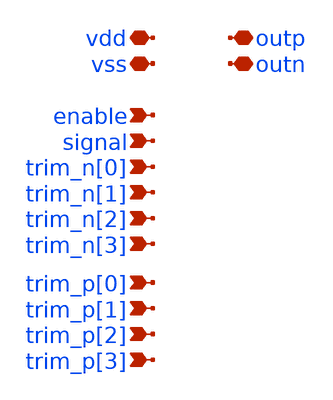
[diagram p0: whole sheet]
** sch_path: xschem/injector_pex_19_8.sch
**.subckt injector_pex_19_8 enable signal trim_n[0] trim_n[1] trim_n[2] trim_n[3] trim_p[0]
*+ trim_p[1] trim_p[2] trim_p[3] vss vdd outp outn
*.ipin enable
*.ipin signal
*.ipin trim_n[0]
*.ipin trim_n[1]
*.ipin trim_n[2]
*.ipin trim_n[3]
*.ipin trim_p[0]
*.ipin trim_p[1]
*.ipin trim_p[2]
*.ipin trim_p[3]
*.iopin vss
*.iopin vdd
*.iopin outp
*.iopin outn
**** begin user architecture code

* NGSPICE file created from injector_flat.ext - technology: gf180mcuC

.subckt injector_flat enable outn outp signal trim_n[0] trim_n[1] trim_n[2] trim_n[3]  trim_p[0]
+ trim_p[1] trim_p[2] trim_p[3] vss vdd
X0 vdd a_9644_7080# a_9556_7124# vdd pmos_6p0 w=1.22u l=1u
X1 outn _00_ vss vss nmos_6p0 w=0.82u l=0.6u
X2 vdd _21_ a_2500_4539# vdd pmos_6p0 w=0.62u l=0.5u
X3 outn _00_ vdd vdd pmos_6p0 w=1.22u l=0.5u
X4 a_2588_5512# a_2500_5556# vss vss nmos_6p0 w=0.82u l=1u
X5 _25_ a_6509_3160# vdd vdd pmos_6p0 w=1.22u l=0.5u
X6 vdd a_3036_5079# a_2948_5176# vdd pmos_6p0 w=1.22u l=1u
X7 a_3044_3229# a_2612_3229# vss vss nmos_6p0 w=0.36u l=0.6u
X8 outp _00_ vdd vdd pmos_6p0 w=1.22u l=0.5u
X9 outp _14_ vdd vdd pmos_6p0 w=1.22u l=0.5u
X10 outn _00_ vss vss nmos_6p0 w=0.82u l=0.6u
X11 vdd _00_ outn vdd pmos_6p0 w=1.22u l=0.5u
X12 vdd _24_ a_7092_3229# vdd pmos_6p0 w=0.62u l=0.5u
X13 vss trim_p[1] a_7204_7933# vss nmos_6p0 w=0.36u l=0.6u
X14 outp _00_ vdd vdd pmos_6p0 w=1.22u l=0.5u
X15 outn _00_ vdd vdd pmos_6p0 w=1.22u l=0.5u
X16 outp _00_ vdd vdd pmos_6p0 w=1.22u l=0.5u
X17 a_2892_7156# trim_p[0] a_2932_7675# vss nmos_6p0 w=0.36u l=0.6u
X18 _00_ enable vdd vdd pmos_6p0 w=1.22u l=0.5u
X19 outn _00_ vdd vdd pmos_6p0 w=1.22u l=0.5u
X20 outp _00_ vdd vdd pmos_6p0 w=1.22u l=0.5u
X21 a_8573_7889# _00_ vss vss nmos_6p0 w=0.36u l=0.6u
X22 vdd _16_ outp vdd pmos_6p0 w=1.22u l=0.5u
X23 a_16812_3944# a_16724_3988# vss vss nmos_6p0 w=0.82u l=1u
X24 vdd _00_ outn vdd pmos_6p0 w=1.22u l=0.5u
X25 vdd a_16924_7080# a_16836_7124# vdd pmos_6p0 w=1.22u l=1u
X26 a_15171_7933# a_14708_7933# vss vss nmos_6p0 w=0.36u l=0.6u
X27 _19_ a_6957_6296# vdd vdd pmos_6p0 w=1.22u l=0.5u
X28 vdd a_6284_7080# a_6196_7124# vdd pmos_6p0 w=1.22u l=1u
X29 vdd a_3484_5079# a_3396_5176# vdd pmos_6p0 w=1.22u l=1u
X30 outn _00_ vdd vdd pmos_6p0 w=1.22u l=0.5u
X31 outp _00_ vdd vdd pmos_6p0 w=1.22u l=0.5u
X32 outp _00_ vss vss nmos_6p0 w=0.82u l=0.6u
X33 outn _13_ vss vss nmos_6p0 w=0.82u l=0.6u
X34 a_16280_3604# trim_n[3] vss vss nmos_6p0 w=0.36u l=0.6u
X35 outp _00_ vdd vdd pmos_6p0 w=1.22u l=0.5u
X36 a_12575_3988# a_12132_4539# vdd vdd pmos_6p0 w=0.62u l=0.5u
X37 vdd _26_ a_11124_3229# vdd pmos_6p0 w=0.62u l=0.5u
X38 outn _15_ vss vss nmos_6p0 w=0.82u l=0.6u
X39 a_3044_3229# a_2612_3229# a_3004_3696# vdd pmos_6p0 w=0.62u l=0.5u
X40 a_5724_5512# a_5636_5556# vss vss nmos_6p0 w=0.82u l=1u
X41 vss _11_ outn vss nmos_6p0 w=0.82u l=0.6u
X42 outn _01_ vss vss nmos_6p0 w=0.82u l=0.6u
X43 outn _00_ vss vss nmos_6p0 w=0.82u l=0.6u
X44 outn _01_ vdd vdd pmos_6p0 w=1.22u l=0.5u
X45 a_3981_7889# _00_ vss vss nmos_6p0 w=0.36u l=0.6u
X46 _09_ a_7629_6296# vdd vdd pmos_6p0 w=1.22u l=0.5u
X47 outp _00_ vss vss nmos_6p0 w=0.82u l=0.6u
X48 outp _00_ vdd vdd pmos_6p0 w=1.22u l=0.5u
X49 signal_n signal vss vss nmos_6p0 w=0.82u l=0.6u
X50 a_15375_7124# a_14932_7675# vdd vdd pmos_6p0 w=0.62u l=0.5u
X51 a_16280_3604# trim_n[3] vdd vdd pmos_6p0 w=0.62u l=0.5u
X52 a_1692_5512# a_1604_5556# vss vss nmos_6p0 w=0.82u l=1u
X53 outn a_7555_4539# vss vss nmos_6p0 w=0.82u l=0.6u
X54 vdd a_2140_5079# a_2052_5176# vdd pmos_6p0 w=1.22u l=1u
X55 outp _00_ vss vss nmos_6p0 w=0.82u l=0.6u
X56 outn _09_ vdd vdd pmos_6p0 w=1.22u l=0.5u
X57 vss a_8328_3604# a_7555_3229# vss nmos_6p0 w=0.36u l=0.6u
X58 a_16851_4797# a_16388_4797# vss vss nmos_6p0 w=0.36u l=0.6u
X59 outp _00_ vdd vdd pmos_6p0 w=1.22u l=0.5u
X60 a_7524_7675# a_7092_7156# vss vss nmos_6p0 w=0.36u l=0.6u
X61 a_15487_3728# a_16280_3604# a_15507_3229# vdd pmos_6p0 w=0.62u l=0.5u
X62 a_12595_4539# a_12132_4539# vss vss nmos_6p0 w=0.36u l=0.6u
X63 outp _00_ vss vss nmos_6p0 w=0.82u l=0.6u
X64 vss trim_n[0] a_2612_3229# vss nmos_6p0 w=0.36u l=0.6u
X65 vss a_3044_3229# outp vss nmos_6p0 w=0.82u l=0.6u
X66 outn a_2963_4539# vss vss nmos_6p0 w=0.82u l=0.6u
X67 outp a_15151_8432# vdd vdd pmos_6p0 w=1.095u l=0.5u
X68 _02_ a_5636_8000# vss vss nmos_6p0 w=0.82u l=0.6u
X69 vdd a_16700_8215# a_16612_8312# vdd pmos_6p0 w=1.22u l=1u
X70 a_12360_8308# trim_p[2] vss vss nmos_6p0 w=0.36u l=0.6u
X71 outn _17_ vss vss nmos_6p0 w=0.82u l=0.6u
X72 a_12780_5079# a_12692_5176# vss vss nmos_6p0 w=0.82u l=1u
X73 a_3036_5512# a_2948_5556# vss vss nmos_6p0 w=0.82u l=1u
X74 a_8973_6296# a_8973_6296# vss vss nmos_6p0 w=0.82u l=0.6u
X75 vdd a_17932_8215# a_17844_8312# vdd pmos_6p0 w=1.22u l=1u
X76 vdd a_4828_5512# a_4740_5556# vdd pmos_6p0 w=1.22u l=1u
X77 a_3505_6296# _00_ vss vss nmos_6p0 w=0.36u l=0.6u
X78 a_1692_7080# a_1604_7124# vss vss nmos_6p0 w=0.82u l=1u
X79 vdd a_8573_7889# a_7596_8400# vdd pmos_6p0 w=0.62u l=0.5u
X80 vdd a_4492_3944# a_4404_3988# vdd pmos_6p0 w=1.22u l=1u
X81 a_2943_3988# a_3736_3976# a_2963_4539# vdd pmos_6p0 w=0.62u l=0.5u
X82 vss a_3505_6296# _04_ vss nmos_6p0 w=0.82u l=0.6u
X83 vdd a_8461_7553# a_7484_7156# vdd pmos_6p0 w=0.62u l=0.5u
X84 a_10541_3160# a_10541_3160# vss vss nmos_6p0 w=0.82u l=0.6u
X85 _08_ a_7517_5512# vdd vdd pmos_6p0 w=1.22u l=0.5u
X86 vss a_2932_7675# outp vss nmos_6p0 w=0.82u l=0.6u
X87 a_1692_6647# a_1604_6744# vss vss nmos_6p0 w=0.82u l=1u
X88 vss trim_p[2] a_12020_7156# vss nmos_6p0 w=0.36u l=0.6u
X89 vss a_16280_3604# a_15507_3229# vss nmos_6p0 w=0.36u l=0.6u
X90 a_2892_7156# trim_p[0] vdd vdd pmos_6p0 w=0.62u l=0.5u
X91 vss a_3044_7933# outn vss nmos_6p0 w=0.82u l=0.6u
X92 outp _00_ vss vss nmos_6p0 w=0.82u l=0.6u
X93 a_3484_5512# a_3396_5556# vss vss nmos_6p0 w=0.82u l=1u
X94 _01_ a_1716_8000# vss vss nmos_6p0 w=0.82u l=0.6u
X95 outp _00_ vss vss nmos_6p0 w=0.82u l=0.6u
X96 vdd a_9644_3944# a_9556_3988# vdd pmos_6p0 w=1.22u l=1u
X97 a_6173_5512# a_6173_5512# vss vss nmos_6p0 w=0.82u l=0.6u
X98 _03_ a_4659_7124# vdd vdd pmos_6p0 w=1.22u l=0.5u
X99 a_5612_6647# a_5524_6744# vss vss nmos_6p0 w=0.82u l=1u
X100 vdd signal a_4847_7124# vdd pmos_6p0 w=0.565u l=0.5u
X101 vdd a_14012_8215# a_13924_8312# vdd pmos_6p0 w=1.22u l=1u
X102 vdd trim_n[1] a_7535_3988# vdd pmos_6p0 w=0.62u l=0.5u
X103 a_12412_7156# trim_p[2] a_12452_7675# vss nmos_6p0 w=0.36u l=0.6u
X104 vdd _03_ a_5636_8000# vdd pmos_6p0 w=0.565u l=0.5u
X105 a_10541_7864# a_10541_7864# vss vss nmos_6p0 w=0.82u l=0.6u
X106 a_6285_6296# a_6285_6296# vss vss nmos_6p0 w=0.82u l=0.6u
X107 a_7555_3229# a_7092_3229# vss vss nmos_6p0 w=0.36u l=0.6u
X108 a_16831_5296# a_17624_5172# a_16851_4797# vdd pmos_6p0 w=0.62u l=0.5u
X109 vdd _11_ outn vdd pmos_6p0 w=1.22u l=0.5u
X110 vss _03_ a_5636_8000# vss nmos_6p0 w=0.36u l=0.6u
X111 a_2140_5512# a_2052_5556# vss vss nmos_6p0 w=0.82u l=1u
X112 vdd a_3932_5512# a_3844_5556# vdd pmos_6p0 w=1.22u l=1u
X113 a_3044_7933# a_2612_7933# a_3004_8400# vdd pmos_6p0 w=0.62u l=0.5u
X114 signal_n signal vdd vdd pmos_6p0 w=1.22u l=0.5u
X115 a_8573_7889# _00_ vdd vdd pmos_6p0 w=0.62u l=0.5u
X116 a_8461_7553# _00_ vdd vdd pmos_6p0 w=0.62u l=0.5u
X117 a_3004_3696# trim_n[0] vdd vdd pmos_6p0 w=0.62u l=0.5u
X118 vss a_12360_8308# a_11587_7933# vss nmos_6p0 w=0.36u l=0.6u
X119 a_3004_3696# trim_n[0] a_3044_3229# vss nmos_6p0 w=0.36u l=0.6u
X120 a_6732_7080# a_6644_7124# vss vss nmos_6p0 w=0.82u l=1u
X121 a_15151_8432# a_14708_7933# vdd vdd pmos_6p0 w=0.62u l=0.5u
X122 vss a_3981_7889# a_3044_7933# vss nmos_6p0 w=0.36u l=0.6u
X123 outp _20_ vss vss nmos_6p0 w=0.82u l=0.6u
X124 outn a_12595_4539# vss vss nmos_6p0 w=0.82u l=0.6u
X125 a_11587_3229# a_11124_3229# vss vss nmos_6p0 w=0.36u l=0.6u
X126 outn _00_ vss vss nmos_6p0 w=0.82u l=0.6u
X127 vdd a_2588_5512# a_2500_5556# vdd pmos_6p0 w=1.22u l=1u
X128 a_3981_7889# _00_ vdd vdd pmos_6p0 w=0.62u l=0.5u
X129 a_3869_7553# _00_ vdd vdd pmos_6p0 w=0.62u l=0.5u
X130 outp _02_ vdd vdd pmos_6p0 w=1.22u l=0.5u
X131 a_15507_3229# trim_n[3] a_15487_3728# vss nmos_6p0 w=0.36u l=0.6u
X132 a_5276_5512# a_5188_5556# vss vss nmos_6p0 w=0.82u l=1u
X133 vss a_3736_3976# a_2963_4539# vss nmos_6p0 w=0.36u l=0.6u
X134 vdd a_7484_7156# outp vdd pmos_6p0 w=1.095u l=0.5u
X135 vdd trim_n[1] a_7535_3728# vdd pmos_6p0 w=0.62u l=0.5u
X136 vdd trim_p[3] a_15375_7124# vdd pmos_6p0 w=0.62u l=0.5u
X137 outp _18_ vdd vdd pmos_6p0 w=1.22u l=0.5u
X138 a_4659_7124# _00_ vss vss nmos_6p0 w=0.36u l=0.6u
X139 a_2140_7080# a_2052_7124# vss vss nmos_6p0 w=0.82u l=1u
X140 vdd a_7596_8400# outn vdd pmos_6p0 w=1.095u l=0.5u
X141 outn _00_ vdd vdd pmos_6p0 w=1.22u l=0.5u
X142 outn _00_ vss vss nmos_6p0 w=0.82u l=0.6u
X143 vdd a_16812_3944# a_16724_3988# vdd pmos_6p0 w=1.22u l=1u
X144 _18_ a_8973_6296# vdd vdd pmos_6p0 w=1.22u l=0.5u
X145 a_16831_5296# a_16388_4797# vdd vdd pmos_6p0 w=0.62u l=0.5u
X146 outn _00_ vss vss nmos_6p0 w=0.82u l=0.6u
X147 a_2140_6647# a_2052_6744# vss vss nmos_6p0 w=0.82u l=1u
X148 outp _12_ vdd vdd pmos_6p0 w=1.22u l=0.5u
X149 _20_ a_10541_3160# vdd vdd pmos_6p0 w=1.22u l=0.5u
X150 a_4829_4728# a_4829_4728# vss vss nmos_6p0 w=0.82u l=0.6u
X151 outn _00_ vdd vdd pmos_6p0 w=1.22u l=0.5u
X152 outp _00_ vdd vdd pmos_6p0 w=1.22u l=0.5u
X153 outp _00_ vss vss nmos_6p0 w=0.82u l=0.6u
X154 vdd _00_ a_14708_7933# vdd pmos_6p0 w=0.62u l=0.5u
X155 a_12452_7675# a_12020_7156# vss vss nmos_6p0 w=0.36u l=0.6u
X156 vdd trim_n[2] a_11567_3728# vdd pmos_6p0 w=0.62u l=0.5u
X157 vdd a_5724_5512# a_5636_5556# vdd pmos_6p0 w=1.22u l=1u
X158 vdd a_1692_6647# a_1604_6744# vdd pmos_6p0 w=1.22u l=1u
X159 outn _00_ vdd vdd pmos_6p0 w=1.22u l=0.5u
X160 a_15395_7675# a_14932_7675# vss vss nmos_6p0 w=0.36u l=0.6u
X161 vdd a_12780_5079# a_12692_5176# vdd pmos_6p0 w=1.22u l=1u
X162 vdd a_1692_5512# a_1604_5556# vdd pmos_6p0 w=1.22u l=1u
X163 a_10093_7080# a_10093_7080# vss vss nmos_6p0 w=0.82u l=0.6u
X164 vdd _27_ a_15044_3229# vdd pmos_6p0 w=0.62u l=0.5u
X165 outp _00_ vdd vdd pmos_6p0 w=1.22u l=0.5u
X166 vdd a_5612_6647# a_5524_6744# vdd pmos_6p0 w=1.22u l=1u
X167 a_11587_7933# trim_p[2] a_11567_8432# vss nmos_6p0 w=0.36u l=0.6u
X168 a_9644_5512# a_9556_5556# vss vss nmos_6p0 w=0.82u l=1u
X169 a_5837_3944# a_5837_3944# vss vss nmos_6p0 w=0.82u l=0.6u
X170 vss _28_ a_16388_4797# vss nmos_6p0 w=0.36u l=0.6u
X171 a_4380_5512# a_4292_5556# vss vss nmos_6p0 w=0.82u l=1u
X172 outn _00_ vss vss nmos_6p0 w=0.82u l=0.6u
X173 outp _14_ vss vss nmos_6p0 w=0.82u l=0.6u
X174 vdd trim_n[2] a_12575_3988# vdd pmos_6p0 w=0.62u l=0.5u
X175 a_7535_3728# a_7092_3229# vdd vdd pmos_6p0 w=0.62u l=0.5u
X176 a_3044_7933# a_2612_7933# vss vss nmos_6p0 w=0.36u l=0.6u
X177 _28_ a_6285_6296# vdd vdd pmos_6p0 w=1.22u l=0.5u
X178 vss _25_ a_12132_4539# vss nmos_6p0 w=0.36u l=0.6u
X179 outp _02_ vss vss nmos_6p0 w=0.82u l=0.6u
X180 a_6509_3944# a_6509_3944# vss vss nmos_6p0 w=0.82u l=0.6u
X181 a_2963_4539# trim_n[0] a_2943_3988# vss nmos_6p0 w=0.36u l=0.6u
X182 vss _02_ outn vss nmos_6p0 w=0.82u l=0.6u
X183 outn _00_ vss vss nmos_6p0 w=0.82u l=0.6u
X184 _00_ enable vss vss nmos_6p0 w=0.82u l=0.6u
X185 vss signal_n a_3505_6296# vss nmos_6p0 w=0.36u l=0.6u
X186 outn _00_ vss vss nmos_6p0 w=0.82u l=0.6u
X187 vdd a_3036_5512# a_2948_5556# vdd pmos_6p0 w=1.22u l=1u
X188 a_3004_8400# trim_p[0] vdd vdd pmos_6p0 w=0.62u l=0.5u
X189 a_11567_3728# a_11124_3229# vdd vdd pmos_6p0 w=0.62u l=0.5u
X190 outn _00_ vss vss nmos_6p0 w=0.82u l=0.6u
X191 a_9644_7080# a_9556_7124# vss vss nmos_6p0 w=0.82u l=1u
X192 outp _00_ vss vss nmos_6p0 w=0.82u l=0.6u
X193 a_15944_8308# trim_p[3] vdd vdd pmos_6p0 w=0.62u l=0.5u
X194 outn _15_ vdd vdd pmos_6p0 w=1.22u l=0.5u
X195 outn _07_ vdd vdd pmos_6p0 w=1.22u l=0.5u
X196 outn _07_ vss vss nmos_6p0 w=0.82u l=0.6u
X197 outn _00_ vdd vdd pmos_6p0 w=1.22u l=0.5u
X198 vdd trim_p[0] a_2500_7156# vdd pmos_6p0 w=0.62u l=0.5u
X199 vss a_3869_7553# a_2932_7675# vss nmos_6p0 w=0.36u l=0.6u
X200 vss a_15944_8308# a_15171_7933# vss nmos_6p0 w=0.36u l=0.6u
X201 outn _00_ vss vss nmos_6p0 w=0.82u l=0.6u
X202 vdd _00_ outp vdd pmos_6p0 w=1.22u l=0.5u
X203 outp _00_ vss vss nmos_6p0 w=0.82u l=0.6u
X204 vss signal a_4659_7124# vss nmos_6p0 w=0.36u l=0.6u
X205 vdd a_3484_5512# a_3396_5556# vdd pmos_6p0 w=1.22u l=1u
X206 outp _10_ vss vss nmos_6p0 w=0.82u l=0.6u
X207 a_12412_7156# trim_p[2] vdd vdd pmos_6p0 w=0.62u l=0.5u
X208 a_15171_7933# trim_p[3] a_15151_8432# vss nmos_6p0 w=0.36u l=0.6u
X209 outn _00_ vdd vdd pmos_6p0 w=1.22u l=0.5u
X210 _17_ a_6173_5512# vdd vdd pmos_6p0 w=1.22u l=0.5u
X211 a_16812_5512# a_16724_5556# vss vss nmos_6p0 w=0.82u l=1u
X212 vss signal signal_n vss nmos_6p0 w=0.82u l=0.6u
X213 vdd a_2140_6647# a_2052_6744# vdd pmos_6p0 w=1.22u l=1u
X214 a_16924_7080# a_16836_7124# vss vss nmos_6p0 w=0.82u l=1u
X215 a_4847_7124# _00_ a_4659_7124# vdd pmos_6p0 w=0.565u l=0.5u
X216 outp _00_ vss vss nmos_6p0 w=0.82u l=0.6u
X217 a_13389_7553# _00_ vdd vdd pmos_6p0 w=0.62u l=0.5u
X218 a_6284_7080# a_6196_7124# vss vss nmos_6p0 w=0.82u l=1u
X219 a_7636_7933# a_7204_7933# a_7596_8400# vdd pmos_6p0 w=0.62u l=0.5u
X220 a_7535_3988# a_8328_3976# a_7555_4539# vdd pmos_6p0 w=0.62u l=0.5u
X221 outp _00_ vdd vdd pmos_6p0 w=1.22u l=0.5u
X222 outp _00_ vss vss nmos_6p0 w=0.82u l=0.6u
X223 vss _23_ a_7092_4539# vss nmos_6p0 w=0.36u l=0.6u
X224 vss trim_p[1] a_7092_7156# vss nmos_6p0 w=0.36u l=0.6u
X225 vdd trim_p[1] a_7204_7933# vdd pmos_6p0 w=0.62u l=0.5u
X226 vdd _00_ a_11124_7933# vdd pmos_6p0 w=0.62u l=0.5u
X227 a_8461_7553# _00_ vss vss nmos_6p0 w=0.36u l=0.6u
X228 a_8328_3976# trim_n[1] vss vss nmos_6p0 w=0.36u l=0.6u
X229 vdd a_2140_5512# a_2052_5556# vdd pmos_6p0 w=1.22u l=1u
X230 vss trim_p[0] a_2612_7933# vss nmos_6p0 w=0.36u l=0.6u
X231 outp _00_ vss vss nmos_6p0 w=0.82u l=0.6u
X232 a_7484_7156# trim_p[1] vdd vdd pmos_6p0 w=0.62u l=0.5u
X233 vdd trim_p[2] a_11567_8432# vdd pmos_6p0 w=0.62u l=0.5u
X234 vdd a_9859_3204# _16_ vdd pmos_6p0 w=1.22u l=0.5u
X235 outn _00_ vdd vdd pmos_6p0 w=1.22u l=0.5u
X236 vss a_7636_7933# outn vss nmos_6p0 w=0.82u l=0.6u
X237 outp _00_ vss vss nmos_6p0 w=0.82u l=0.6u
X238 vdd a_15683_4472# _06_ vdd pmos_6p0 w=1.22u l=0.5u
X239 a_6957_4728# a_6957_4728# vss vss nmos_6p0 w=0.82u l=0.6u
X240 outn _19_ vdd vdd pmos_6p0 w=1.22u l=0.5u
X241 outp _00_ vss vss nmos_6p0 w=0.82u l=0.6u
X242 a_3736_3976# trim_n[0] vss vss nmos_6p0 w=0.36u l=0.6u
X243 _27_ a_4829_4728# vdd vdd pmos_6p0 w=1.22u l=0.5u
X244 a_3869_7553# _00_ vss vss nmos_6p0 w=0.36u l=0.6u
X245 vss _26_ a_11124_3229# vss nmos_6p0 w=0.36u l=0.6u
X246 a_7629_4728# a_7629_4728# vss vss nmos_6p0 w=0.82u l=0.6u
X247 outp _00_ vdd vdd pmos_6p0 w=1.22u l=0.5u
X248 outp _00_ vss vss nmos_6p0 w=0.82u l=0.6u
X249 vdd a_5276_5512# a_5188_5556# vdd pmos_6p0 w=1.22u l=1u
X250 a_7535_3728# a_8328_3604# a_7555_3229# vdd pmos_6p0 w=0.62u l=0.5u
X251 vdd a_3981_3185# a_3004_3696# vdd pmos_6p0 w=0.62u l=0.5u
X252 a_15375_7124# a_16168_7112# a_15395_7675# vdd pmos_6p0 w=0.62u l=0.5u
X253 a_15507_3229# a_15044_3229# vss vss nmos_6p0 w=0.36u l=0.6u
X254 outp a_7535_3728# vdd vdd pmos_6p0 w=1.095u l=0.5u
X255 a_12780_6647# a_12692_6744# vss vss nmos_6p0 w=0.82u l=1u
X256 vss a_8573_7889# a_7636_7933# vss nmos_6p0 w=0.36u l=0.6u
X257 a_3505_6296# signal_n a_3897_6875# vdd pmos_6p0 w=0.565u l=0.5u
X258 vdd _23_ a_7092_4539# vdd pmos_6p0 w=0.62u l=0.5u
X259 outp a_7555_3229# vss vss nmos_6p0 w=0.82u l=0.6u
X260 outp a_16831_5296# vdd vdd pmos_6p0 w=1.095u l=0.5u
X261 a_15944_8308# trim_p[3] vss vss nmos_6p0 w=0.36u l=0.6u
X262 a_10205_3944# a_10205_3944# vss vss nmos_6p0 w=0.82u l=0.6u
X263 outp a_11567_3728# vdd vdd pmos_6p0 w=1.095u l=0.5u
X264 a_14684_3511# a_14596_3608# vss vss nmos_6p0 w=0.82u l=1u
X265 vss _00_ a_14932_7675# vss nmos_6p0 w=0.36u l=0.6u
X266 vdd a_3869_7553# a_2892_7156# vdd pmos_6p0 w=0.62u l=0.5u
X267 a_12595_4539# trim_n[2] a_12575_3988# vss nmos_6p0 w=0.36u l=0.6u
X268 a_17932_3511# a_17844_3608# vss vss nmos_6p0 w=0.82u l=1u
X269 _03_ a_4659_7124# vss vss nmos_6p0 w=0.82u l=0.6u
X270 vdd trim_n[3] a_15487_3728# vdd pmos_6p0 w=0.62u l=0.5u
X271 outp _08_ vdd vdd pmos_6p0 w=1.22u l=0.5u
X272 a_3004_8400# trim_p[0] a_3044_7933# vss nmos_6p0 w=0.36u l=0.6u
X273 vdd a_9644_5512# a_9556_5556# vdd pmos_6p0 w=1.22u l=1u
X274 a_2943_3988# a_2500_4539# vdd vdd pmos_6p0 w=0.62u l=0.5u
X275 _15_ a_5837_3944# vdd vdd pmos_6p0 w=1.22u l=0.5u
X276 vdd a_4380_5512# a_4292_5556# vdd pmos_6p0 w=1.22u l=1u
X277 a_11587_7933# a_11124_7933# vss vss nmos_6p0 w=0.36u l=0.6u
X278 outn _05_ vdd vdd pmos_6p0 w=1.22u l=0.5u
X279 outp a_11587_3229# vss vss nmos_6p0 w=0.82u l=0.6u
X280 outn a_15487_3728# vdd vdd pmos_6p0 w=1.095u l=0.5u
X281 a_12575_3988# a_13368_3976# a_12595_4539# vdd pmos_6p0 w=0.62u l=0.5u
X282 outn _00_ vdd vdd pmos_6p0 w=1.22u l=0.5u
X283 _07_ a_6509_3944# vdd vdd pmos_6p0 w=1.22u l=0.5u
X284 outp _00_ vss vss nmos_6p0 w=0.82u l=0.6u
X285 _02_ a_5636_8000# vdd vdd pmos_6p0 w=1.22u l=0.5u
X286 a_16700_8215# a_16612_8312# vss vss nmos_6p0 w=0.82u l=1u
X287 a_13368_3976# trim_n[2] vss vss nmos_6p0 w=0.36u l=0.6u
X288 vss _06_ outp vss nmos_6p0 w=0.82u l=0.6u
X289 a_17932_8215# a_17844_8312# vss vss nmos_6p0 w=0.82u l=1u
X290 a_2963_4539# a_2500_4539# vss vss nmos_6p0 w=0.36u l=0.6u
X291 outn _00_ vdd vdd pmos_6p0 w=1.22u l=0.5u
X292 outn _00_ vss vss nmos_6p0 w=0.82u l=0.6u
X293 outn _00_ vdd vdd pmos_6p0 w=1.22u l=0.5u
X294 outp _00_ vdd vdd pmos_6p0 w=1.22u l=0.5u
X295 outn _13_ vdd vdd pmos_6p0 w=1.22u l=0.5u
X296 a_2932_7675# a_2500_7156# a_2892_7156# vdd pmos_6p0 w=0.62u l=0.5u
X297 vdd trim_p[3] a_15151_8432# vdd pmos_6p0 w=0.62u l=0.5u
X298 outp a_11587_7933# vss vss nmos_6p0 w=0.82u l=0.6u
X299 a_5165_3944# a_5165_3944# vss vss nmos_6p0 w=0.82u l=0.6u
X300 a_7636_7933# a_7204_7933# vss vss nmos_6p0 w=0.36u l=0.6u
X301 a_4045_4728# a_4045_4728# vss vss nmos_6p0 w=0.82u l=0.6u
X302 outn _00_ vdd vdd pmos_6p0 w=1.22u l=0.5u
X303 vss a_12452_7675# outn vss nmos_6p0 w=0.82u l=0.6u
X304 a_2588_5079# a_2500_5176# vss vss nmos_6p0 w=0.82u l=1u
X305 a_7555_4539# trim_n[1] a_7535_3988# vss nmos_6p0 w=0.36u l=0.6u
X306 vss _01_ outp vss nmos_6p0 w=0.82u l=0.6u
X307 a_15487_3728# a_15044_3229# vdd vdd pmos_6p0 w=0.62u l=0.5u
X308 outp _00_ vdd vdd pmos_6p0 w=1.22u l=0.5u
X309 a_13389_7553# _00_ vss vss nmos_6p0 w=0.36u l=0.6u
X310 _01_ a_1716_8000# vdd vdd pmos_6p0 w=1.22u l=0.5u
X311 outp a_11567_8432# vdd vdd pmos_6p0 w=1.095u l=0.5u
X312 outn a_12575_3988# vdd vdd pmos_6p0 w=1.095u l=0.5u
X313 vdd trim_p[2] a_12020_7156# vdd pmos_6p0 w=0.62u l=0.5u
X314 outp _00_ vss vss nmos_6p0 w=0.82u l=0.6u
X315 a_8328_3976# trim_n[1] vdd vdd pmos_6p0 w=0.62u l=0.5u
X316 _05_ a_6957_4728# vdd vdd pmos_6p0 w=1.22u l=0.5u
X317 vdd a_16812_5512# a_16724_5556# vdd pmos_6p0 w=1.22u l=1u
X318 vdd a_12780_6647# a_12692_6744# vdd pmos_6p0 w=1.22u l=1u
X319 outp _00_ vdd vdd pmos_6p0 w=1.22u l=0.5u
X320 a_14012_8215# a_13924_8312# vss vss nmos_6p0 w=0.82u l=1u
X321 outn _00_ vss vss nmos_6p0 w=0.82u l=0.6u
X322 vdd a_3505_6296# _04_ vdd pmos_6p0 w=1.22u l=0.5u
X323 _10_ a_10541_7864# vdd vdd pmos_6p0 w=1.22u l=0.5u
X324 outn a_15375_7124# vdd vdd pmos_6p0 w=1.095u l=0.5u
X325 a_4829_3160# a_4829_3160# vss vss nmos_6p0 w=0.82u l=0.6u
X326 vdd trim_n[3] a_16831_5296# vdd pmos_6p0 w=0.62u l=0.5u
X327 vdd a_2892_7156# outp vdd pmos_6p0 w=1.095u l=0.5u
X328 vss a_7524_7675# outp vss nmos_6p0 w=0.82u l=0.6u
X329 _13_ a_7629_4728# vdd vdd pmos_6p0 w=1.22u l=0.5u
X330 a_3981_3185# _22_ vss vss nmos_6p0 w=0.36u l=0.6u
X331 vss a_17624_5172# a_16851_4797# vss nmos_6p0 w=0.36u l=0.6u
X332 a_3897_6875# _00_ vdd vdd pmos_6p0 w=0.565u l=0.5u
X333 vdd _25_ a_12132_4539# vdd pmos_6p0 w=0.62u l=0.5u
X334 outp _18_ vss vss nmos_6p0 w=0.82u l=0.6u
X335 a_3736_3976# trim_n[0] vdd vdd pmos_6p0 w=0.62u l=0.5u
X336 vss _24_ a_7092_3229# vss nmos_6p0 w=0.36u l=0.6u
X337 vdd a_14684_3511# a_14596_3608# vdd pmos_6p0 w=1.22u l=1u
X338 vss a_13368_3976# a_12595_4539# vss nmos_6p0 w=0.36u l=0.6u
X339 vdd a_17932_3511# a_17844_3608# vdd pmos_6p0 w=1.22u l=1u
X340 a_8328_3604# trim_n[1] vss vss nmos_6p0 w=0.36u l=0.6u
X341 vdd a_1692_7080# a_1604_7124# vdd pmos_6p0 w=1.22u l=1u
X342 vdd trim_n[0] a_2612_3229# vdd pmos_6p0 w=0.62u l=0.5u
X343 vdd _00_ a_14932_7675# vdd pmos_6p0 w=0.62u l=0.5u
X344 outp _12_ vss vss nmos_6p0 w=0.82u l=0.6u
X345 a_1692_5079# a_1604_5176# vss vss nmos_6p0 w=0.82u l=1u
X346 outn _00_ vss vss nmos_6p0 w=0.82u l=0.6u
X347 outn _00_ vss vss nmos_6p0 w=0.82u l=0.6u
X348 a_8328_3604# trim_n[1] vdd vdd pmos_6p0 w=0.62u l=0.5u
X349 a_16168_7112# trim_p[3] vdd vdd pmos_6p0 w=0.62u l=0.5u
X350 a_12360_3604# trim_n[2] vss vss nmos_6p0 w=0.36u l=0.6u
X351 outn a_7535_3988# vdd vdd pmos_6p0 w=1.095u l=0.5u
X352 outp a_16851_4797# vss vss nmos_6p0 w=0.82u l=0.6u
X353 outn _00_ vss vss nmos_6p0 w=0.82u l=0.6u
X354 outn _17_ vdd vdd pmos_6p0 w=1.22u l=0.5u
X355 a_5612_5079# a_5524_5176# vss vss nmos_6p0 w=0.82u l=1u
X356 vss _16_ outp vss nmos_6p0 w=0.82u l=0.6u
X357 outn _00_ vss vss nmos_6p0 w=0.82u l=0.6u
X358 outn _09_ vss vss nmos_6p0 w=0.82u l=0.6u
X359 vss _27_ a_15044_3229# vss nmos_6p0 w=0.36u l=0.6u
X360 a_2932_7675# a_2500_7156# vss vss nmos_6p0 w=0.36u l=0.6u
X361 a_17624_5172# trim_n[3] vdd vdd pmos_6p0 w=0.62u l=0.5u
X362 a_15395_7675# trim_p[3] a_15375_7124# vss nmos_6p0 w=0.36u l=0.6u
X363 a_11567_8432# a_11124_7933# vdd vdd pmos_6p0 w=0.62u l=0.5u
X364 a_12360_3604# trim_n[2] vdd vdd pmos_6p0 w=0.62u l=0.5u
X365 a_3036_5079# a_2948_5176# vss vss nmos_6p0 w=0.82u l=1u
X366 outn _00_ vdd vdd pmos_6p0 w=1.22u l=0.5u
X367 outn a_2943_3988# vdd vdd pmos_6p0 w=1.095u l=0.5u
X368 a_7596_8400# trim_p[1] a_7636_7933# vss nmos_6p0 w=0.36u l=0.6u
X369 _12_ a_10205_3944# vdd vdd pmos_6p0 w=1.22u l=0.5u
X370 a_11567_3728# a_12360_3604# a_11587_3229# vdd pmos_6p0 w=0.62u l=0.5u
X371 a_16851_4797# trim_n[3] a_16831_5296# vss nmos_6p0 w=0.36u l=0.6u
X372 vss a_8328_3976# a_7555_4539# vss nmos_6p0 w=0.36u l=0.6u
X373 vdd _01_ outp vdd pmos_6p0 w=1.22u l=0.5u
X374 a_15151_8432# a_15944_8308# a_15171_7933# vdd pmos_6p0 w=0.62u l=0.5u
X375 a_5837_3160# a_5837_3160# vss vss nmos_6p0 w=0.82u l=0.6u
X376 vss a_15683_4472# a_15683_4472# vss nmos_6p0 w=0.82u l=0.6u
X377 outp _00_ vdd vdd pmos_6p0 w=1.22u l=0.5u
X378 outp _00_ vdd vdd pmos_6p0 w=1.22u l=0.5u
X379 a_2029_3160# a_2029_3160# vss vss nmos_6p0 w=0.82u l=0.6u
X380 a_16168_7112# trim_p[3] vss vss nmos_6p0 w=0.36u l=0.6u
X381 vdd a_6732_7080# a_6644_7124# vdd pmos_6p0 w=1.22u l=1u
X382 outp a_15171_7933# vss vss nmos_6p0 w=0.82u l=0.6u
X383 outn _19_ vss vss nmos_6p0 w=0.82u l=0.6u
X384 outp _00_ vss vss nmos_6p0 w=0.82u l=0.6u
X385 a_3484_5079# a_3396_5176# vss vss nmos_6p0 w=0.82u l=1u
X386 a_13368_3976# trim_n[2] vdd vdd pmos_6p0 w=0.62u l=0.5u
X387 vdd a_13389_7553# a_12412_7156# vdd pmos_6p0 w=0.62u l=0.5u
X388 a_6509_3160# a_6509_3160# vss vss nmos_6p0 w=0.82u l=0.6u
X389 outp _00_ vdd vdd pmos_6p0 w=1.22u l=0.5u
X390 _23_ a_4829_3160# vdd vdd pmos_6p0 w=1.22u l=0.5u
X391 a_3981_3185# _22_ vdd vdd pmos_6p0 w=0.62u l=0.5u
X392 vss _00_ outn vss nmos_6p0 w=0.82u l=0.6u
X393 vss _00_ a_11124_7933# vss nmos_6p0 w=0.36u l=0.6u
X394 vdd a_3004_3696# outp vdd pmos_6p0 w=1.095u l=0.5u
X395 _22_ a_4045_4728# vdd vdd pmos_6p0 w=1.22u l=0.5u
X396 vdd _02_ outn vdd pmos_6p0 w=1.22u l=0.5u
X397 vdd a_2140_7080# a_2052_7124# vdd pmos_6p0 w=1.22u l=1u
X398 vdd a_2588_5079# a_2500_5176# vdd pmos_6p0 w=1.22u l=1u
X399 vdd a_9859_7908# _11_ vdd pmos_6p0 w=1.22u l=0.5u
X400 vss a_12360_3604# a_11587_3229# vss nmos_6p0 w=0.36u l=0.6u
X401 outn a_15507_3229# vss vss nmos_6p0 w=0.82u l=0.6u
X402 a_4828_5512# a_4740_5556# vss vss nmos_6p0 w=0.82u l=1u
X403 vdd a_12412_7156# outn vdd pmos_6p0 w=1.095u l=0.5u
X404 vss _00_ outn vss nmos_6p0 w=0.82u l=0.6u
X405 a_2140_5079# a_2052_5176# vss vss nmos_6p0 w=0.82u l=1u
X406 vdd _06_ outp vdd pmos_6p0 w=1.22u l=0.5u
X407 vss a_3981_3185# a_3044_3229# vss nmos_6p0 w=0.36u l=0.6u
X408 vss trim_p[0] a_2500_7156# vss nmos_6p0 w=0.36u l=0.6u
X409 a_4492_3944# a_4404_3988# vss vss nmos_6p0 w=0.82u l=1u
X410 vss _21_ a_2500_4539# vss nmos_6p0 w=0.36u l=0.6u
X411 a_6957_6296# a_6957_6296# vss vss nmos_6p0 w=0.82u l=0.6u
X412 outp _20_ vdd vdd pmos_6p0 w=1.22u l=0.5u
X413 vdd trim_n[0] a_2943_3988# vdd pmos_6p0 w=0.62u l=0.5u
X414 a_7517_5512# a_7517_5512# vss vss nmos_6p0 w=0.82u l=0.6u
X415 a_7535_3988# a_7092_4539# vdd vdd pmos_6p0 w=0.62u l=0.5u
X416 vdd trim_p[0] a_2612_7933# vdd pmos_6p0 w=0.62u l=0.5u
X417 _24_ a_5165_3944# vdd vdd pmos_6p0 w=1.22u l=0.5u
X418 a_7629_6296# a_7629_6296# vss vss nmos_6p0 w=0.82u l=0.6u
X419 outn a_15395_7675# vss vss nmos_6p0 w=0.82u l=0.6u
X420 vss _00_ outp vss nmos_6p0 w=0.82u l=0.6u
X421 vss a_9859_3204# a_9859_3204# vss nmos_6p0 w=0.82u l=0.6u
X422 vdd _04_ a_1716_8000# vdd pmos_6p0 w=0.565u l=0.5u
X423 a_12452_7675# a_12020_7156# a_12412_7156# vdd pmos_6p0 w=0.62u l=0.5u
X424 vdd a_3981_7889# a_3004_8400# vdd pmos_6p0 w=0.62u l=0.5u
X425 vss a_13389_7553# a_12452_7675# vss nmos_6p0 w=0.36u l=0.6u
X426 _14_ a_10093_7080# vdd vdd pmos_6p0 w=1.22u l=0.5u
X427 vss _04_ a_1716_8000# vss nmos_6p0 w=0.36u l=0.6u
X428 a_9644_3944# a_9556_3988# vss vss nmos_6p0 w=0.82u l=1u
X429 a_7555_3229# trim_n[1] a_7535_3728# vss nmos_6p0 w=0.36u l=0.6u
X430 a_7555_4539# a_7092_4539# vss vss nmos_6p0 w=0.36u l=0.6u
X431 vdd _28_ a_16388_4797# vdd pmos_6p0 w=0.62u l=0.5u
X432 vss a_16168_7112# a_15395_7675# vss nmos_6p0 w=0.36u l=0.6u
X433 a_7596_8400# trim_p[1] vdd vdd pmos_6p0 w=0.62u l=0.5u
X434 outn _05_ vss vss nmos_6p0 w=0.82u l=0.6u
X435 a_17624_5172# trim_n[3] vss vss nmos_6p0 w=0.36u l=0.6u
X436 vdd a_1692_5079# a_1604_5176# vdd pmos_6p0 w=1.22u l=1u
X437 vss _00_ a_14708_7933# vss nmos_6p0 w=0.36u l=0.6u
X438 outn _00_ vdd vdd pmos_6p0 w=1.22u l=0.5u
X439 a_7524_7675# a_7092_7156# a_7484_7156# vdd pmos_6p0 w=0.62u l=0.5u
X440 a_12360_8308# trim_p[2] vdd vdd pmos_6p0 w=0.62u l=0.5u
X441 a_3932_5512# a_3844_5556# vss vss nmos_6p0 w=0.82u l=1u
X442 outn _00_ vdd vdd pmos_6p0 w=1.22u l=0.5u
X443 vdd a_3004_8400# outn vdd pmos_6p0 w=1.095u l=0.5u
X444 vss a_9859_7908# a_9859_7908# vss nmos_6p0 w=0.82u l=0.6u
X445 _26_ a_5837_3160# vdd vdd pmos_6p0 w=1.22u l=0.5u
X446 vss a_8461_7553# a_7524_7675# vss nmos_6p0 w=0.36u l=0.6u
X447 vdd trim_p[1] a_7092_7156# vdd pmos_6p0 w=0.62u l=0.5u
X448 a_11567_8432# a_12360_8308# a_11587_7933# vdd pmos_6p0 w=0.62u l=0.5u
X449 _21_ a_2029_3160# vdd vdd pmos_6p0 w=1.22u l=0.5u
X450 outp _10_ vdd vdd pmos_6p0 w=1.22u l=0.5u
X451 outp _08_ vss vss nmos_6p0 w=0.82u l=0.6u
X452 vdd a_5612_5079# a_5524_5176# vdd pmos_6p0 w=1.22u l=1u
X453 a_11587_3229# trim_n[2] a_11567_3728# vss nmos_6p0 w=0.36u l=0.6u
X454 a_7484_7156# trim_p[1] a_7524_7675# vss nmos_6p0 w=0.36u l=0.6u
X455 vdd signal signal_n vdd pmos_6p0 w=1.22u l=0.5u
C0 _07_ _27_ 3.98fF
C1 _00_ outp 7.47fF
C2 outp vdd 6.22fF
C3 _18_ _19_ 4.06fF
C4 _00_ vdd 3.48fF
C5 outn outp 3.02fF
C6 _09_ outn 2.74fF
C7 _00_ _14_ 3.64fF
C8 _25_ _26_ 2.52fF
C9 _00_ outn 6.65fF
C10 outn vdd 5.77fF
C11 _18_ _12_ 3.27fF
C12 _28_ _14_ 3.34fF
C13 _27_ outn 3.00fF
C14 _28_ outn 3.58fF
C15 _05_ outp 2.40fF
C16 _09_ outp 2.48fF
C17 trim_n[2] vss 2.73fF
C18 trim_n[1] vss 2.79fF
C19 trim_n[0] vss 2.61fF
C20 trim_n[3] vss 3.02fF
C21 trim_p[3] vss 2.67fF
C22 trim_p[2] vss 2.71fF
C23 trim_p[1] vss 2.64fF
C24 outp vss 7.77fF
C25 outn vss 7.18fF
C26 trim_p[0] vss 2.57fF
C27 vdd vss 175.97fF
C28 _00_ vss 22.00fF $ **FLOATING
.ends


XDUT enable outn outp signal trim_n[0] trim_n[1] trim_n[2] trim_n[3]  trim_p[0] trim_p[1] trim_p[2]
+ trim_p[3] vss vdd injector_flat


**** end user architecture code
**.ends
.end
